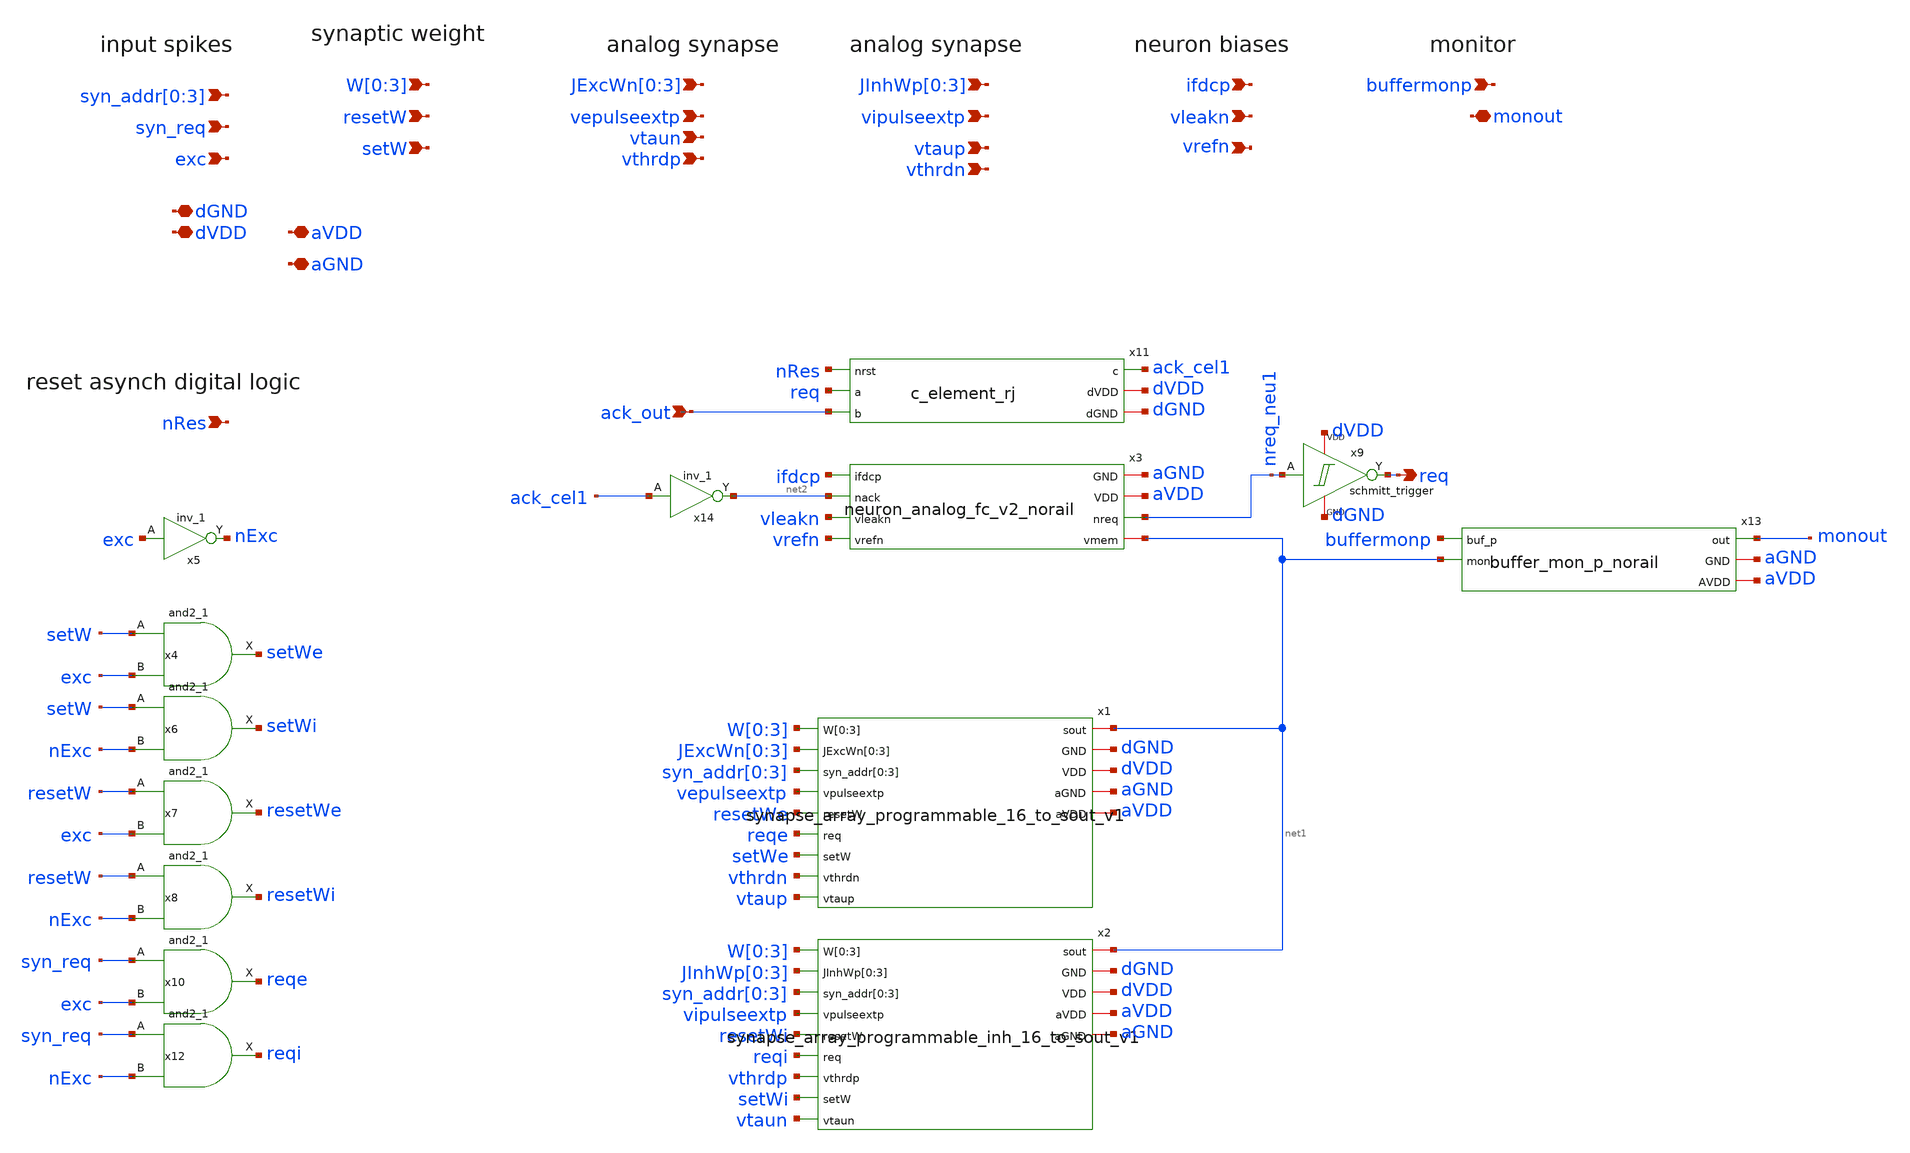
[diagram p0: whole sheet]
** sch_path: design/xschem/neuron_32syn_v1_norail.sch
**.subckt neuron_32syn_v1_norail ack_out dGND dVDD vepulseextp
*+ syn_addr[0],syn_addr[1],syn_addr[2],syn_addr[3] W[0],W[1],W[2],W[3] setW resetW syn_req exc vipulseextp req vleakn ifdcp vrefn nRes aVDD buffermonp
*+ monout JExcWn[0],JExcWn[1],JExcWn[2],JExcWn[3] JInhWp[0],JInhWp[1],JInhWp[2],JInhWp[3] vtaun vthrdp vtaup
*+ vthrdn aGND
*.ipin ack_out
*.iopin dGND
*.iopin dVDD
*.ipin vepulseextp
*.ipin syn_addr[0],syn_addr[1],syn_addr[2],syn_addr[3]
*.ipin W[0],W[1],W[2],W[3]
*.ipin setW
*.ipin resetW
*.ipin syn_req
*.ipin exc
*.ipin vipulseextp
*.opin req
*.ipin vleakn
*.ipin ifdcp
*.ipin vrefn
*.ipin nRes
*.iopin aVDD
*.ipin buffermonp
*.iopin monout
*.ipin JExcWn[0],JExcWn[1],JExcWn[2],JExcWn[3]
*.ipin JInhWp[0],JInhWp[1],JInhWp[2],JInhWp[3]
*.ipin vtaun
*.ipin vthrdp
*.ipin vtaup
*.ipin vthrdn
*.iopin aGND
x11 nRes req ack_out ack_cel1 dVDD dGND c_element_rj
x4 setW exc dGND dGND dVDD dVDD setWe sky130_fd_sc_hd__and2_1
x5 exc dGND dGND dVDD dVDD nExc sky130_fd_sc_hd__inv_1
x6 setW nExc dGND dGND dVDD dVDD setWi sky130_fd_sc_hd__and2_1
x7 resetW exc dGND dGND dVDD dVDD resetWe sky130_fd_sc_hd__and2_1
x8 resetW nExc dGND dGND dVDD dVDD resetWi sky130_fd_sc_hd__and2_1
x10 syn_req exc dGND dGND dVDD dVDD reqe sky130_fd_sc_hd__and2_1
x12 syn_req nExc dGND dGND dVDD dVDD reqi sky130_fd_sc_hd__and2_1
x14 ack_cel1 dGND dGND dVDD dVDD net2 sky130_fd_sc_hd__inv_1
x1 W[0] W[1] W[2] W[3] JExcWn[0] JExcWn[1] JExcWn[2] JExcWn[3] net1 syn_addr[0] syn_addr[1]
+ syn_addr[2] syn_addr[3] vepulseextp resetWe reqe setWe vthrdn vtaup dGND dVDD aGND aVDD
+ synapse_array_programmable_16_to_sout_v1
x2 net1 W[0] W[1] W[2] W[3] JInhWp[0] JInhWp[1] JInhWp[2] JInhWp[3] syn_addr[0] syn_addr[1]
+ syn_addr[2] syn_addr[3] vipulseextp resetWi reqi vthrdp setWi vtaun dGND dVDD aVDD aGND
+ synapse_array_programmable_inh_16_to_sout_v1
x9 nreq_neu1 req dVDD dGND schmitt_trigger
x3 aGND aVDD nreq_neu1 ifdcp net2 net1 vleakn vrefn neuron_analog_fc_v2_norail
x13 buffermonp monout net1 aGND aVDD buffer_mon_p_norail
**.ends

* expanding   symbol:  c_element_rj.sym # of pins=6
** sym_path: design/xschem/c_element_rj.sym
** sch_path: design/xschem/c_element_rj.sch
.subckt c_element_rj nrst a b c dVDD dGND
*.iopin dGND
*.iopin dVDD
*.opin c
*.ipin b
*.ipin a
*.ipin nrst
XM14 c net6 dVDD dVDD sky130_fd_pr__pfet_01v8 L=0.15 W=1 nf=1 ad='int((nf+1)/2) * W/nf * 0.29' as='int((nf+2)/2) * W/nf * 0.29'
+ pd='2*int((nf+1)/2) * (W/nf + 0.29)' ps='2*int((nf+2)/2) * (W/nf + 0.29)' nrd='0.29 / W' nrs='0.29 / W'
+ sa=0 sb=0 sd=0 mult=1 m=1
XM5 net6 nrst dVDD dVDD sky130_fd_pr__pfet_01v8 L=0.15 W=1 nf=1 ad='int((nf+1)/2) * W/nf * 0.29' as='int((nf+2)/2) * W/nf * 0.29'
+ pd='2*int((nf+1)/2) * (W/nf + 0.29)' ps='2*int((nf+2)/2) * (W/nf + 0.29)' nrd='0.29 / W' nrs='0.29 / W'
+ sa=0 sb=0 sd=0 mult=1 m=1
XM6 net5 b dVDD dVDD sky130_fd_pr__pfet_01v8 L=0.15 W=1 nf=1 ad='int((nf+1)/2) * W/nf * 0.29' as='int((nf+2)/2) * W/nf * 0.29'
+ pd='2*int((nf+1)/2) * (W/nf + 0.29)' ps='2*int((nf+2)/2) * (W/nf + 0.29)' nrd='0.29 / W' nrs='0.29 / W'
+ sa=0 sb=0 sd=0 mult=1 m=1
XM4 net4 a dVDD dVDD sky130_fd_pr__pfet_01v8 L=0.15 W=1 nf=1 ad='int((nf+1)/2) * W/nf * 0.29' as='int((nf+2)/2) * W/nf * 0.29'
+ pd='2*int((nf+1)/2) * (W/nf + 0.29)' ps='2*int((nf+2)/2) * (W/nf + 0.29)' nrd='0.29 / W' nrs='0.29 / W'
+ sa=0 sb=0 sd=0 mult=1 m=1
XM7 net3 b net4 dVDD sky130_fd_pr__pfet_01v8 L=0.15 W=1 nf=1 ad='int((nf+1)/2) * W/nf * 0.29' as='int((nf+2)/2) * W/nf * 0.29'
+ pd='2*int((nf+1)/2) * (W/nf + 0.29)' ps='2*int((nf+2)/2) * (W/nf + 0.29)' nrd='0.29 / W' nrs='0.29 / W'
+ sa=0 sb=0 sd=0 mult=1 m=1
XM8 net3 a net5 dVDD sky130_fd_pr__pfet_01v8 L=0.15 W=1 nf=1 ad='int((nf+1)/2) * W/nf * 0.29' as='int((nf+2)/2) * W/nf * 0.29'
+ pd='2*int((nf+1)/2) * (W/nf + 0.29)' ps='2*int((nf+2)/2) * (W/nf + 0.29)' nrd='0.29 / W' nrs='0.29 / W'
+ sa=0 sb=0 sd=0 mult=1 m=1
XM10 net5 c net4 dVDD sky130_fd_pr__pfet_01v8 L=0.15 W=1 nf=1 ad='int((nf+1)/2) * W/nf * 0.29' as='int((nf+2)/2) * W/nf * 0.29'
+ pd='2*int((nf+1)/2) * (W/nf + 0.29)' ps='2*int((nf+2)/2) * (W/nf + 0.29)' nrd='0.29 / W' nrs='0.29 / W'
+ sa=0 sb=0 sd=0 mult=1 m=1
XM12 c net6 dGND dGND sky130_fd_pr__nfet_01v8 L=0.15 W=0.65 nf=1 ad='int((nf+1)/2) * W/nf * 0.29' as='int((nf+2)/2) * W/nf * 0.29'
+ pd='2*int((nf+1)/2) * (W/nf + 0.29)' ps='2*int((nf+2)/2) * (W/nf + 0.29)' nrd='0.29 / W' nrs='0.29 / W'
+ sa=0 sb=0 sd=0 mult=1 m=1
XM1 net3 nrst net6 dGND sky130_fd_pr__nfet_01v8 L=0.15 W=0.65 nf=1 ad='int((nf+1)/2) * W/nf * 0.29' as='int((nf+2)/2) * W/nf * 0.29'
+ pd='2*int((nf+1)/2) * (W/nf + 0.29)' ps='2*int((nf+2)/2) * (W/nf + 0.29)' nrd='0.29 / W' nrs='0.29 / W'
+ sa=0 sb=0 sd=0 mult=1 m=1
XM2 net3 b net1 dGND sky130_fd_pr__nfet_01v8 L=0.15 W=0.65 nf=1 ad='int((nf+1)/2) * W/nf * 0.29' as='int((nf+2)/2) * W/nf * 0.29'
+ pd='2*int((nf+1)/2) * (W/nf + 0.29)' ps='2*int((nf+2)/2) * (W/nf + 0.29)' nrd='0.29 / W' nrs='0.29 / W'
+ sa=0 sb=0 sd=0 mult=1 m=1
XM3 net3 a net2 dGND sky130_fd_pr__nfet_01v8 L=0.15 W=0.65 nf=1 ad='int((nf+1)/2) * W/nf * 0.29' as='int((nf+2)/2) * W/nf * 0.29'
+ pd='2*int((nf+1)/2) * (W/nf + 0.29)' ps='2*int((nf+2)/2) * (W/nf + 0.29)' nrd='0.29 / W' nrs='0.29 / W'
+ sa=0 sb=0 sd=0 mult=1 m=1
XM9 net2 c net1 dGND sky130_fd_pr__nfet_01v8 L=0.15 W=0.65 nf=1 ad='int((nf+1)/2) * W/nf * 0.29' as='int((nf+2)/2) * W/nf * 0.29'
+ pd='2*int((nf+1)/2) * (W/nf + 0.29)' ps='2*int((nf+2)/2) * (W/nf + 0.29)' nrd='0.29 / W' nrs='0.29 / W'
+ sa=0 sb=0 sd=0 mult=1 m=1
XM11 net1 a dGND dGND sky130_fd_pr__nfet_01v8 L=0.15 W=0.65 nf=1 ad='int((nf+1)/2) * W/nf * 0.29' as='int((nf+2)/2) * W/nf * 0.29'
+ pd='2*int((nf+1)/2) * (W/nf + 0.29)' ps='2*int((nf+2)/2) * (W/nf + 0.29)' nrd='0.29 / W' nrs='0.29 / W'
+ sa=0 sb=0 sd=0 mult=1 m=1
XM13 net2 b dGND dGND sky130_fd_pr__nfet_01v8 L=0.15 W=0.65 nf=1 ad='int((nf+1)/2) * W/nf * 0.29' as='int((nf+2)/2) * W/nf * 0.29'
+ pd='2*int((nf+1)/2) * (W/nf + 0.29)' ps='2*int((nf+2)/2) * (W/nf + 0.29)' nrd='0.29 / W' nrs='0.29 / W'
+ sa=0 sb=0 sd=0 mult=1 m=1
.ends


* expanding   symbol:  synapse_array_programmable_16_to_sout_v1.sym # of pins=14
** sym_path: design/xschem/synapse_array_programmable_16_to_sout_v1.sym
** sch_path: design/xschem/synapse_array_programmable_16_to_sout_v1.sch
.subckt synapse_array_programmable_16_to_sout_v1 W[0] W[1] W[2] W[3] JExcWn[0] JExcWn[1] JExcWn[2]
+ JExcWn[3] sout syn_addr[0] syn_addr[1] syn_addr[2] syn_addr[3] vpulseextp resetW req setW vthrdn vtaup GND
+ VDD aGND aVDD
*.iopin GND
*.iopin VDD
*.ipin vpulseextp
*.ipin syn_addr[0],syn_addr[1],syn_addr[2],syn_addr[3]
*.ipin W[0],W[1],W[2],W[3]
*.ipin JExcWn[0],JExcWn[1],JExcWn[2],JExcWn[3]
*.iopin sout
*.ipin setW
*.ipin resetW
*.ipin req
*.ipin vthrdn
*.ipin vtaup
*.iopin aVDD
*.iopin aGND
x3 syn_addr[0] syn_addr[1] syn_addr[2] syn_addr[3] D[0] D[1] D[2] D[3] D[4] D[5] D[6] D[7] D[8] D[9]
+ D[10] D[11] D[12] D[13] D[14] D[15] req req_syn VDD GND decoder_4_to_16
x2[0] req_syn D[0] GND GND VDD VDD net1[15] sky130_fd_sc_hd__and2_1
x2[1] req_syn D[1] GND GND VDD VDD net1[14] sky130_fd_sc_hd__and2_1
x2[2] req_syn D[2] GND GND VDD VDD net1[13] sky130_fd_sc_hd__and2_1
x2[3] req_syn D[3] GND GND VDD VDD net1[12] sky130_fd_sc_hd__and2_1
x2[4] req_syn D[4] GND GND VDD VDD net1[11] sky130_fd_sc_hd__and2_1
x2[5] req_syn D[5] GND GND VDD VDD net1[10] sky130_fd_sc_hd__and2_1
x2[6] req_syn D[6] GND GND VDD VDD net1[9] sky130_fd_sc_hd__and2_1
x2[7] req_syn D[7] GND GND VDD VDD net1[8] sky130_fd_sc_hd__and2_1
x2[8] req_syn D[8] GND GND VDD VDD net1[7] sky130_fd_sc_hd__and2_1
x2[9] req_syn D[9] GND GND VDD VDD net1[6] sky130_fd_sc_hd__and2_1
x2[10] req_syn D[10] GND GND VDD VDD net1[5] sky130_fd_sc_hd__and2_1
x2[11] req_syn D[11] GND GND VDD VDD net1[4] sky130_fd_sc_hd__and2_1
x2[12] req_syn D[12] GND GND VDD VDD net1[3] sky130_fd_sc_hd__and2_1
x2[13] req_syn D[13] GND GND VDD VDD net1[2] sky130_fd_sc_hd__and2_1
x2[14] req_syn D[14] GND GND VDD VDD net1[1] sky130_fd_sc_hd__and2_1
x2[15] req_syn D[15] GND GND VDD VDD net1[0] sky130_fd_sc_hd__and2_1
x1[0] sout JExcWn[0] JExcWn[1] JExcWn[2] JExcWn[3] net1[15] resetW vpulseextp net2[15] vthrdn W[0]
+ W[1] W[2] W[3] vtaup VDD GND aVDD aGND synapse_4bit_memory_v1_norail
x1[1] sout JExcWn[0] JExcWn[1] JExcWn[2] JExcWn[3] net1[14] resetW vpulseextp net2[14] vthrdn W[0]
+ W[1] W[2] W[3] vtaup VDD GND aVDD aGND synapse_4bit_memory_v1_norail
x1[2] sout JExcWn[0] JExcWn[1] JExcWn[2] JExcWn[3] net1[13] resetW vpulseextp net2[13] vthrdn W[0]
+ W[1] W[2] W[3] vtaup VDD GND aVDD aGND synapse_4bit_memory_v1_norail
x1[3] sout JExcWn[0] JExcWn[1] JExcWn[2] JExcWn[3] net1[12] resetW vpulseextp net2[12] vthrdn W[0]
+ W[1] W[2] W[3] vtaup VDD GND aVDD aGND synapse_4bit_memory_v1_norail
x1[4] sout JExcWn[0] JExcWn[1] JExcWn[2] JExcWn[3] net1[11] resetW vpulseextp net2[11] vthrdn W[0]
+ W[1] W[2] W[3] vtaup VDD GND aVDD aGND synapse_4bit_memory_v1_norail
x1[5] sout JExcWn[0] JExcWn[1] JExcWn[2] JExcWn[3] net1[10] resetW vpulseextp net2[10] vthrdn W[0]
+ W[1] W[2] W[3] vtaup VDD GND aVDD aGND synapse_4bit_memory_v1_norail
x1[6] sout JExcWn[0] JExcWn[1] JExcWn[2] JExcWn[3] net1[9] resetW vpulseextp net2[9] vthrdn W[0]
+ W[1] W[2] W[3] vtaup VDD GND aVDD aGND synapse_4bit_memory_v1_norail
x1[7] sout JExcWn[0] JExcWn[1] JExcWn[2] JExcWn[3] net1[8] resetW vpulseextp net2[8] vthrdn W[0]
+ W[1] W[2] W[3] vtaup VDD GND aVDD aGND synapse_4bit_memory_v1_norail
x1[8] sout JExcWn[0] JExcWn[1] JExcWn[2] JExcWn[3] net1[7] resetW vpulseextp net2[7] vthrdn W[0]
+ W[1] W[2] W[3] vtaup VDD GND aVDD aGND synapse_4bit_memory_v1_norail
x1[9] sout JExcWn[0] JExcWn[1] JExcWn[2] JExcWn[3] net1[6] resetW vpulseextp net2[6] vthrdn W[0]
+ W[1] W[2] W[3] vtaup VDD GND aVDD aGND synapse_4bit_memory_v1_norail
x1[10] sout JExcWn[0] JExcWn[1] JExcWn[2] JExcWn[3] net1[5] resetW vpulseextp net2[5] vthrdn W[0]
+ W[1] W[2] W[3] vtaup VDD GND aVDD aGND synapse_4bit_memory_v1_norail
x1[11] sout JExcWn[0] JExcWn[1] JExcWn[2] JExcWn[3] net1[4] resetW vpulseextp net2[4] vthrdn W[0]
+ W[1] W[2] W[3] vtaup VDD GND aVDD aGND synapse_4bit_memory_v1_norail
x1[12] sout JExcWn[0] JExcWn[1] JExcWn[2] JExcWn[3] net1[3] resetW vpulseextp net2[3] vthrdn W[0]
+ W[1] W[2] W[3] vtaup VDD GND aVDD aGND synapse_4bit_memory_v1_norail
x1[13] sout JExcWn[0] JExcWn[1] JExcWn[2] JExcWn[3] net1[2] resetW vpulseextp net2[2] vthrdn W[0]
+ W[1] W[2] W[3] vtaup VDD GND aVDD aGND synapse_4bit_memory_v1_norail
x1[14] sout JExcWn[0] JExcWn[1] JExcWn[2] JExcWn[3] net1[1] resetW vpulseextp net2[1] vthrdn W[0]
+ W[1] W[2] W[3] vtaup VDD GND aVDD aGND synapse_4bit_memory_v1_norail
x1[15] sout JExcWn[0] JExcWn[1] JExcWn[2] JExcWn[3] net1[0] resetW vpulseextp net2[0] vthrdn W[0]
+ W[1] W[2] W[3] vtaup VDD GND aVDD aGND synapse_4bit_memory_v1_norail
x3[0] D[0] setW GND GND VDD VDD net2[15] sky130_fd_sc_hd__and2_1
x3[1] D[1] setW GND GND VDD VDD net2[14] sky130_fd_sc_hd__and2_1
x3[2] D[2] setW GND GND VDD VDD net2[13] sky130_fd_sc_hd__and2_1
x3[3] D[3] setW GND GND VDD VDD net2[12] sky130_fd_sc_hd__and2_1
x3[4] D[4] setW GND GND VDD VDD net2[11] sky130_fd_sc_hd__and2_1
x3[5] D[5] setW GND GND VDD VDD net2[10] sky130_fd_sc_hd__and2_1
x3[6] D[6] setW GND GND VDD VDD net2[9] sky130_fd_sc_hd__and2_1
x3[7] D[7] setW GND GND VDD VDD net2[8] sky130_fd_sc_hd__and2_1
x3[8] D[8] setW GND GND VDD VDD net2[7] sky130_fd_sc_hd__and2_1
x3[9] D[9] setW GND GND VDD VDD net2[6] sky130_fd_sc_hd__and2_1
x3[10] D[10] setW GND GND VDD VDD net2[5] sky130_fd_sc_hd__and2_1
x3[11] D[11] setW GND GND VDD VDD net2[4] sky130_fd_sc_hd__and2_1
x3[12] D[12] setW GND GND VDD VDD net2[3] sky130_fd_sc_hd__and2_1
x3[13] D[13] setW GND GND VDD VDD net2[2] sky130_fd_sc_hd__and2_1
x3[14] D[14] setW GND GND VDD VDD net2[1] sky130_fd_sc_hd__and2_1
x3[15] D[15] setW GND GND VDD VDD net2[0] sky130_fd_sc_hd__and2_1
.ends


* expanding   symbol:  synapse_array_programmable_inh_16_to_sout_v1.sym # of pins=14
** sym_path: design/xschem/synapse_array_programmable_inh_16_to_sout_v1.sym
** sch_path: design/xschem/synapse_array_programmable_inh_16_to_sout_v1.sch
.subckt synapse_array_programmable_inh_16_to_sout_v1 sout W[0] W[1] W[2] W[3] JInhWp[0] JInhWp[1]
+ JInhWp[2] JInhWp[3] syn_addr[0] syn_addr[1] syn_addr[2] syn_addr[3] vpulseextp resetW req vthrdp setW vtaun
+ GND VDD aVDD aGND
*.ipin vpulseextp
*.ipin syn_addr[0],syn_addr[1],syn_addr[2],syn_addr[3]
*.ipin W[0],W[1],W[2],W[3]
*.ipin JInhWp[0],JInhWp[1],JInhWp[2],JInhWp[3]
*.iopin sout
*.ipin setW
*.ipin resetW
*.ipin req
*.ipin vthrdp
*.ipin vtaun
*.iopin GND
*.iopin VDD
*.iopin aVDD
*.iopin aGND
x3 syn_addr[0] syn_addr[1] syn_addr[2] syn_addr[3] D[0] D[1] D[2] D[3] D[4] D[5] D[6] D[7] D[8] D[9]
+ D[10] D[11] D[12] D[13] D[14] D[15] req req_syn VDD GND decoder_4_to_16
x2[0] req_syn D[0] GND GND VDD VDD net1[15] sky130_fd_sc_hd__and2_1
x2[1] req_syn D[1] GND GND VDD VDD net1[14] sky130_fd_sc_hd__and2_1
x2[2] req_syn D[2] GND GND VDD VDD net1[13] sky130_fd_sc_hd__and2_1
x2[3] req_syn D[3] GND GND VDD VDD net1[12] sky130_fd_sc_hd__and2_1
x2[4] req_syn D[4] GND GND VDD VDD net1[11] sky130_fd_sc_hd__and2_1
x2[5] req_syn D[5] GND GND VDD VDD net1[10] sky130_fd_sc_hd__and2_1
x2[6] req_syn D[6] GND GND VDD VDD net1[9] sky130_fd_sc_hd__and2_1
x2[7] req_syn D[7] GND GND VDD VDD net1[8] sky130_fd_sc_hd__and2_1
x2[8] req_syn D[8] GND GND VDD VDD net1[7] sky130_fd_sc_hd__and2_1
x2[9] req_syn D[9] GND GND VDD VDD net1[6] sky130_fd_sc_hd__and2_1
x2[10] req_syn D[10] GND GND VDD VDD net1[5] sky130_fd_sc_hd__and2_1
x2[11] req_syn D[11] GND GND VDD VDD net1[4] sky130_fd_sc_hd__and2_1
x2[12] req_syn D[12] GND GND VDD VDD net1[3] sky130_fd_sc_hd__and2_1
x2[13] req_syn D[13] GND GND VDD VDD net1[2] sky130_fd_sc_hd__and2_1
x2[14] req_syn D[14] GND GND VDD VDD net1[1] sky130_fd_sc_hd__and2_1
x2[15] req_syn D[15] GND GND VDD VDD net1[0] sky130_fd_sc_hd__and2_1
x3[0] D[0] setW GND GND VDD VDD net2[15] sky130_fd_sc_hd__and2_1
x3[1] D[1] setW GND GND VDD VDD net2[14] sky130_fd_sc_hd__and2_1
x3[2] D[2] setW GND GND VDD VDD net2[13] sky130_fd_sc_hd__and2_1
x3[3] D[3] setW GND GND VDD VDD net2[12] sky130_fd_sc_hd__and2_1
x3[4] D[4] setW GND GND VDD VDD net2[11] sky130_fd_sc_hd__and2_1
x3[5] D[5] setW GND GND VDD VDD net2[10] sky130_fd_sc_hd__and2_1
x3[6] D[6] setW GND GND VDD VDD net2[9] sky130_fd_sc_hd__and2_1
x3[7] D[7] setW GND GND VDD VDD net2[8] sky130_fd_sc_hd__and2_1
x3[8] D[8] setW GND GND VDD VDD net2[7] sky130_fd_sc_hd__and2_1
x3[9] D[9] setW GND GND VDD VDD net2[6] sky130_fd_sc_hd__and2_1
x3[10] D[10] setW GND GND VDD VDD net2[5] sky130_fd_sc_hd__and2_1
x3[11] D[11] setW GND GND VDD VDD net2[4] sky130_fd_sc_hd__and2_1
x3[12] D[12] setW GND GND VDD VDD net2[3] sky130_fd_sc_hd__and2_1
x3[13] D[13] setW GND GND VDD VDD net2[2] sky130_fd_sc_hd__and2_1
x3[14] D[14] setW GND GND VDD VDD net2[1] sky130_fd_sc_hd__and2_1
x3[15] D[15] setW GND GND VDD VDD net2[0] sky130_fd_sc_hd__and2_1
x1[0] sout JInhWp[0] JInhWp[1] JInhWp[2] JInhWp[3] resetW net1[15] vpulseextp net2[15] vthrdp W[0]
+ W[1] W[2] W[3] vtaun GND VDD aVDD aGND synapse_4bit_memory_inh_v1_norail
x1[1] sout JInhWp[0] JInhWp[1] JInhWp[2] JInhWp[3] resetW net1[14] vpulseextp net2[14] vthrdp W[0]
+ W[1] W[2] W[3] vtaun GND VDD aVDD aGND synapse_4bit_memory_inh_v1_norail
x1[2] sout JInhWp[0] JInhWp[1] JInhWp[2] JInhWp[3] resetW net1[13] vpulseextp net2[13] vthrdp W[0]
+ W[1] W[2] W[3] vtaun GND VDD aVDD aGND synapse_4bit_memory_inh_v1_norail
x1[3] sout JInhWp[0] JInhWp[1] JInhWp[2] JInhWp[3] resetW net1[12] vpulseextp net2[12] vthrdp W[0]
+ W[1] W[2] W[3] vtaun GND VDD aVDD aGND synapse_4bit_memory_inh_v1_norail
x1[4] sout JInhWp[0] JInhWp[1] JInhWp[2] JInhWp[3] resetW net1[11] vpulseextp net2[11] vthrdp W[0]
+ W[1] W[2] W[3] vtaun GND VDD aVDD aGND synapse_4bit_memory_inh_v1_norail
x1[5] sout JInhWp[0] JInhWp[1] JInhWp[2] JInhWp[3] resetW net1[10] vpulseextp net2[10] vthrdp W[0]
+ W[1] W[2] W[3] vtaun GND VDD aVDD aGND synapse_4bit_memory_inh_v1_norail
x1[6] sout JInhWp[0] JInhWp[1] JInhWp[2] JInhWp[3] resetW net1[9] vpulseextp net2[9] vthrdp W[0]
+ W[1] W[2] W[3] vtaun GND VDD aVDD aGND synapse_4bit_memory_inh_v1_norail
x1[7] sout JInhWp[0] JInhWp[1] JInhWp[2] JInhWp[3] resetW net1[8] vpulseextp net2[8] vthrdp W[0]
+ W[1] W[2] W[3] vtaun GND VDD aVDD aGND synapse_4bit_memory_inh_v1_norail
x1[8] sout JInhWp[0] JInhWp[1] JInhWp[2] JInhWp[3] resetW net1[7] vpulseextp net2[7] vthrdp W[0]
+ W[1] W[2] W[3] vtaun GND VDD aVDD aGND synapse_4bit_memory_inh_v1_norail
x1[9] sout JInhWp[0] JInhWp[1] JInhWp[2] JInhWp[3] resetW net1[6] vpulseextp net2[6] vthrdp W[0]
+ W[1] W[2] W[3] vtaun GND VDD aVDD aGND synapse_4bit_memory_inh_v1_norail
x1[10] sout JInhWp[0] JInhWp[1] JInhWp[2] JInhWp[3] resetW net1[5] vpulseextp net2[5] vthrdp W[0]
+ W[1] W[2] W[3] vtaun GND VDD aVDD aGND synapse_4bit_memory_inh_v1_norail
x1[11] sout JInhWp[0] JInhWp[1] JInhWp[2] JInhWp[3] resetW net1[4] vpulseextp net2[4] vthrdp W[0]
+ W[1] W[2] W[3] vtaun GND VDD aVDD aGND synapse_4bit_memory_inh_v1_norail
x1[12] sout JInhWp[0] JInhWp[1] JInhWp[2] JInhWp[3] resetW net1[3] vpulseextp net2[3] vthrdp W[0]
+ W[1] W[2] W[3] vtaun GND VDD aVDD aGND synapse_4bit_memory_inh_v1_norail
x1[13] sout JInhWp[0] JInhWp[1] JInhWp[2] JInhWp[3] resetW net1[2] vpulseextp net2[2] vthrdp W[0]
+ W[1] W[2] W[3] vtaun GND VDD aVDD aGND synapse_4bit_memory_inh_v1_norail
x1[14] sout JInhWp[0] JInhWp[1] JInhWp[2] JInhWp[3] resetW net1[1] vpulseextp net2[1] vthrdp W[0]
+ W[1] W[2] W[3] vtaun GND VDD aVDD aGND synapse_4bit_memory_inh_v1_norail
x1[15] sout JInhWp[0] JInhWp[1] JInhWp[2] JInhWp[3] resetW net1[0] vpulseextp net2[0] vthrdp W[0]
+ W[1] W[2] W[3] vtaun GND VDD aVDD aGND synapse_4bit_memory_inh_v1_norail
.ends


* expanding   symbol:  schmitt_trigger.sym # of pins=4
** sym_path: design/xschem/schmitt_trigger.sym
** sch_path: design/xschem/schmitt_trigger.sch
.subckt schmitt_trigger A Y VDD GND
*.ipin A
*.opin Y
*.iopin VDD
*.iopin GND
XM3 net2 A GND GND sky130_fd_pr__nfet_01v8 L=0.15 W=0.65 nf=1 ad='int((nf+1)/2) * W/nf * 0.29' as='int((nf+2)/2) * W/nf * 0.29'
+ pd='2*int((nf+1)/2) * (W/nf + 0.29)' ps='2*int((nf+2)/2) * (W/nf + 0.29)' nrd='0.29 / W' nrs='0.29 / W'
+ sa=0 sb=0 sd=0 mult=1 m=1
XM1 Y A net2 GND sky130_fd_pr__nfet_01v8 L=0.15 W=0.65 nf=1 ad='int((nf+1)/2) * W/nf * 0.29' as='int((nf+2)/2) * W/nf * 0.29'
+ pd='2*int((nf+1)/2) * (W/nf + 0.29)' ps='2*int((nf+2)/2) * (W/nf + 0.29)' nrd='0.29 / W' nrs='0.29 / W'
+ sa=0 sb=0 sd=0 mult=1 m=1
XM7 VDD Y net2 GND sky130_fd_pr__nfet_01v8 L=0.15 W=0.42 nf=1 ad='int((nf+1)/2) * W/nf * 0.29' as='int((nf+2)/2) * W/nf * 0.29'
+ pd='2*int((nf+1)/2) * (W/nf + 0.29)' ps='2*int((nf+2)/2) * (W/nf + 0.29)' nrd='0.29 / W' nrs='0.29 / W'
+ sa=0 sb=0 sd=0 mult=1 m=1
XM4 net1 A VDD VDD sky130_fd_pr__pfet_01v8 L=0.15 W=1 nf=1 ad='int((nf+1)/2) * W/nf * 0.29' as='int((nf+2)/2) * W/nf * 0.29'
+ pd='2*int((nf+1)/2) * (W/nf + 0.29)' ps='2*int((nf+2)/2) * (W/nf + 0.29)' nrd='0.29 / W' nrs='0.29 / W'
+ sa=0 sb=0 sd=0 mult=1 m=1
XM2 Y A net1 VDD sky130_fd_pr__pfet_01v8 L=0.15 W=1 nf=1 ad='int((nf+1)/2) * W/nf * 0.29' as='int((nf+2)/2) * W/nf * 0.29'
+ pd='2*int((nf+1)/2) * (W/nf + 0.29)' ps='2*int((nf+2)/2) * (W/nf + 0.29)' nrd='0.29 / W' nrs='0.29 / W'
+ sa=0 sb=0 sd=0 mult=1 m=1
XM5 GND Y net1 VDD sky130_fd_pr__pfet_01v8 L=0.15 W=0.82 nf=1 ad='int((nf+1)/2) * W/nf * 0.29' as='int((nf+2)/2) * W/nf * 0.29'
+ pd='2*int((nf+1)/2) * (W/nf + 0.29)' ps='2*int((nf+2)/2) * (W/nf + 0.29)' nrd='0.29 / W' nrs='0.29 / W'
+ sa=0 sb=0 sd=0 mult=1 m=1
.ends


* expanding   symbol:  neuron_analog_fc_v2_norail.sym # of pins=8
** sym_path: design/xschem/neuron_analog_fc_v2_norail.sym
** sch_path: design/xschem/neuron_analog_fc_v2_norail.sch
.subckt neuron_analog_fc_v2_norail GND VDD nreq ifdcp nack vmem vleakn vrefn
*.ipin vleakn
*.iopin GND
*.iopin VDD
*.opin nreq
*.ipin vrefn
*.ipin nack
*.ipin ifdcp
*.iopin vmem
XC1 GND vmem sky130_fd_pr__cap_mim_m3_1 W=5 L=5 MF=1 m=1
XM1 vmem ifdcp VDD VDD sky130_fd_pr__pfet_01v8 L=2.0 W=1.0 nf=1 ad='int((nf+1)/2) * W/nf * 0.29' as='int((nf+2)/2) * W/nf * 0.29'
+ pd='2*int((nf+1)/2) * (W/nf + 0.29)' ps='2*int((nf+2)/2) * (W/nf + 0.29)' nrd='0.29 / W' nrs='0.29 / W'
+ sa=0 sb=0 sd=0 mult=1 m=1
XM5 net2 nreq VDD VDD sky130_fd_pr__pfet_01v8 L=0.25 W=1.0 nf=1 ad='int((nf+1)/2) * W/nf * 0.29' as='int((nf+2)/2) * W/nf * 0.29'
+ pd='2*int((nf+1)/2) * (W/nf + 0.29)' ps='2*int((nf+2)/2) * (W/nf + 0.29)' nrd='0.29 / W' nrs='0.29 / W'
+ sa=0 sb=0 sd=0 mult=1 m=1
XM7 net3 nreq net4 GND sky130_fd_pr__nfet_01v8 L=0.15 W=0.6 nf=1 ad='int((nf+1)/2) * W/nf * 0.29' as='int((nf+2)/2) * W/nf * 0.29'
+ pd='2*int((nf+1)/2) * (W/nf + 0.29)' ps='2*int((nf+2)/2) * (W/nf + 0.29)' nrd='0.29 / W' nrs='0.29 / W'
+ sa=0 sb=0 sd=0 mult=1 m=1
XM6 net5 nack VDD VDD sky130_fd_pr__pfet_01v8 L=0.25 W=1.0 nf=1 ad='int((nf+1)/2) * W/nf * 0.29' as='int((nf+2)/2) * W/nf * 0.29'
+ pd='2*int((nf+1)/2) * (W/nf + 0.29)' ps='2*int((nf+2)/2) * (W/nf + 0.29)' nrd='0.29 / W' nrs='0.29 / W'
+ sa=0 sb=0 sd=0 mult=1 m=1
XM9 nreq vmem net2 VDD sky130_fd_pr__pfet_01v8 L=0.15 W=1.0 nf=1 ad='int((nf+1)/2) * W/nf * 0.29' as='int((nf+2)/2) * W/nf * 0.29'
+ pd='2*int((nf+1)/2) * (W/nf + 0.29)' ps='2*int((nf+2)/2) * (W/nf + 0.29)' nrd='0.29 / W' nrs='0.29 / W'
+ sa=0 sb=0 sd=0 mult=1 m=1
XM10 net3 nreq net5 VDD sky130_fd_pr__pfet_01v8 L=0.15 W=1.0 nf=1 ad='int((nf+1)/2) * W/nf * 0.29' as='int((nf+2)/2) * W/nf * 0.29'
+ pd='2*int((nf+1)/2) * (W/nf + 0.29)' ps='2*int((nf+2)/2) * (W/nf + 0.29)' nrd='0.29 / W' nrs='0.29 / W'
+ sa=0 sb=0 sd=0 mult=1 m=1
XM4 vmem nreq VDD VDD sky130_fd_pr__pfet_01v8 L=1.0 W=1.0 nf=1 ad='int((nf+1)/2) * W/nf * 0.29' as='int((nf+2)/2) * W/nf * 0.29'
+ pd='2*int((nf+1)/2) * (W/nf + 0.29)' ps='2*int((nf+2)/2) * (W/nf + 0.29)' nrd='0.29 / W' nrs='0.29 / W'
+ sa=0 sb=0 sd=0 mult=1 m=1
XM2 nreq vmem net1 GND sky130_fd_pr__nfet_01v8 L=0.15 W=0.6 nf=1 ad='int((nf+1)/2) * W/nf * 0.29' as='int((nf+2)/2) * W/nf * 0.29'
+ pd='2*int((nf+1)/2) * (W/nf + 0.29)' ps='2*int((nf+2)/2) * (W/nf + 0.29)' nrd='0.29 / W' nrs='0.29 / W'
+ sa=0 sb=0 sd=0 mult=1 m=1
XM3 net4 vrefn GND GND sky130_fd_pr__nfet_01v8 L=1.0 W=0.6 nf=1 ad='int((nf+1)/2) * W/nf * 0.29' as='int((nf+2)/2) * W/nf * 0.29'
+ pd='2*int((nf+1)/2) * (W/nf + 0.29)' ps='2*int((nf+2)/2) * (W/nf + 0.29)' nrd='0.29 / W' nrs='0.29 / W'
+ sa=0 sb=0 sd=0 mult=1 m=1
XM8 net1 net1 GND GND sky130_fd_pr__nfet_01v8 L=0.15 W=0.6 nf=1 ad='int((nf+1)/2) * W/nf * 0.29' as='int((nf+2)/2) * W/nf * 0.29'
+ pd='2*int((nf+1)/2) * (W/nf + 0.29)' ps='2*int((nf+2)/2) * (W/nf + 0.29)' nrd='0.29 / W' nrs='0.29 / W'
+ sa=0 sb=0 sd=0 mult=1 m=1
XM11 vmem net3 GND GND sky130_fd_pr__nfet_01v8 L=0.2 W=1.0 nf=1 ad='int((nf+1)/2) * W/nf * 0.29' as='int((nf+2)/2) * W/nf * 0.29'
+ pd='2*int((nf+1)/2) * (W/nf + 0.29)' ps='2*int((nf+2)/2) * (W/nf + 0.29)' nrd='0.29 / W' nrs='0.29 / W'
+ sa=0 sb=0 sd=0 mult=1 m=1
XM12 vmem vleakn GND GND sky130_fd_pr__nfet_01v8 L=2.0 W=1.0 nf=1 ad='int((nf+1)/2) * W/nf * 0.29' as='int((nf+2)/2) * W/nf * 0.29'
+ pd='2*int((nf+1)/2) * (W/nf + 0.29)' ps='2*int((nf+2)/2) * (W/nf + 0.29)' nrd='0.29 / W' nrs='0.29 / W'
+ sa=0 sb=0 sd=0 mult=1 m=1
XM13 GND net3 GND GND sky130_fd_pr__nfet_01v8 L=2.0 W=1.0 nf=1 ad='int((nf+1)/2) * W/nf * 0.29' as='int((nf+2)/2) * W/nf * 0.29'
+ pd='2*int((nf+1)/2) * (W/nf + 0.29)' ps='2*int((nf+2)/2) * (W/nf + 0.29)' nrd='0.29 / W' nrs='0.29 / W'
+ sa=0 sb=0 sd=0 mult=1 m=1
.ends


* expanding   symbol:  buffer_mon_p_norail.sym # of pins=5
** sym_path: design/xschem/buffer_mon_p_norail.sym
** sch_path: design/xschem/buffer_mon_p_norail.sch
.subckt buffer_mon_p_norail buf_p out mon GND AVDD
*.iopin GND
*.iopin AVDD
*.ipin buf_p
*.ipin mon
*.opin out
XM1 out out net2 AVDD sky130_fd_pr__pfet_01v8 L=0.5 W=1.0 nf=1 ad='int((nf+1)/2) * W/nf * 0.29' as='int((nf+2)/2) * W/nf * 0.29'
+ pd='2*int((nf+1)/2) * (W/nf + 0.29)' ps='2*int((nf+2)/2) * (W/nf + 0.29)' nrd='0.29 / W' nrs='0.29 / W'
+ sa=0 sb=0 sd=0 mult=1 m=1
XM5 net1 mon net2 AVDD sky130_fd_pr__pfet_01v8 L=0.5 W=1.0 nf=1 ad='int((nf+1)/2) * W/nf * 0.29' as='int((nf+2)/2) * W/nf * 0.29'
+ pd='2*int((nf+1)/2) * (W/nf + 0.29)' ps='2*int((nf+2)/2) * (W/nf + 0.29)' nrd='0.29 / W' nrs='0.29 / W'
+ sa=0 sb=0 sd=0 mult=1 m=1
XM2 net2 buf_p AVDD AVDD sky130_fd_pr__pfet_01v8 L=0.30 W=1.0 nf=1 ad='int((nf+1)/2) * W/nf * 0.29' as='int((nf+2)/2) * W/nf * 0.29'
+ pd='2*int((nf+1)/2) * (W/nf + 0.29)' ps='2*int((nf+2)/2) * (W/nf + 0.29)' nrd='0.29 / W' nrs='0.29 / W'
+ sa=0 sb=0 sd=0 mult=1 m=1
XM3 out net1 GND GND sky130_fd_pr__nfet_01v8 L=0.5 W=1.0 nf=1 ad='int((nf+1)/2) * W/nf * 0.29' as='int((nf+2)/2) * W/nf * 0.29'
+ pd='2*int((nf+1)/2) * (W/nf + 0.29)' ps='2*int((nf+2)/2) * (W/nf + 0.29)' nrd='0.29 / W' nrs='0.29 / W'
+ sa=0 sb=0 sd=0 mult=1 m=1
XM4 net1 net1 GND GND sky130_fd_pr__nfet_01v8 L=0.5 W=1.0 nf=1 ad='int((nf+1)/2) * W/nf * 0.29' as='int((nf+2)/2) * W/nf * 0.29'
+ pd='2*int((nf+1)/2) * (W/nf + 0.29)' ps='2*int((nf+2)/2) * (W/nf + 0.29)' nrd='0.29 / W' nrs='0.29 / W'
+ sa=0 sb=0 sd=0 mult=1 m=1
.ends


* expanding   symbol:  decoder_4_to_16.sym # of pins=6
** sym_path: design/xschem/decoder_4_to_16.sym
** sch_path: design/xschem/decoder_4_to_16.sch
.subckt decoder_4_to_16 A[0] A[1] A[2] A[3] D[0] D[1] D[2] D[3] D[4] D[5] D[6] D[7] D[8] D[9] D[10]
+ D[11] D[12] D[13] D[14] D[15] req req_syn dVDD dGND
*.ipin A[0],A[1],A[2],A[3]
*.ipin req
*.opin D[0],D[1],D[2],D[3],D[4],D[5],D[6],D[7],D[8],D[9],D[10],D[11],D[12],D[13],D[14],D[15]
*.opin req_syn
*.iopin dVDD
*.iopin dGND
x21 req dGND dGND dVDD dVDD net5 sky130_fd_sc_hd__inv_1
x22 net5 dGND dGND dVDD dVDD net6 sky130_fd_sc_hd__inv_1
x23 net6 dGND dGND dVDD dVDD net7 sky130_fd_sc_hd__inv_1
x24 net7 dGND dGND dVDD dVDD req_syn sky130_fd_sc_hd__inv_1
x20 A[3] A[2] A[1] A[0] dGND dGND dVDD dVDD D[15] sky130_fd_sc_hd__and4_1
x19 A[3] A[2] A[1] net4 dGND dGND dVDD dVDD D[14] sky130_fd_sc_hd__and4_1
x18 A[3] A[2] net3 A[0] dGND dGND dVDD dVDD D[13] sky130_fd_sc_hd__and4_1
x17 A[3] A[2] net3 net4 dGND dGND dVDD dVDD D[12] sky130_fd_sc_hd__and4_1
x16 A[3] net2 A[1] A[0] dGND dGND dVDD dVDD D[11] sky130_fd_sc_hd__and4_1
x15 A[3] net2 A[1] net4 dGND dGND dVDD dVDD D[10] sky130_fd_sc_hd__and4_1
x13 A[3] net2 net3 A[0] dGND dGND dVDD dVDD D[9] sky130_fd_sc_hd__and4_1
x4 A[3] net2 net3 net4 dGND dGND dVDD dVDD D[8] sky130_fd_sc_hd__and4_1
x5 net1 A[2] A[1] A[0] dGND dGND dVDD dVDD D[7] sky130_fd_sc_hd__and4_1
x6 net1 A[2] A[1] net4 dGND dGND dVDD dVDD D[6] sky130_fd_sc_hd__and4_1
x8 net1 A[2] net3 net4 dGND dGND dVDD dVDD D[4] sky130_fd_sc_hd__and4_1
x9 net1 net2 A[1] net4 dGND dGND dVDD dVDD D[2] sky130_fd_sc_hd__and4_1
x10 net1 net2 net3 net4 dGND dGND dVDD dVDD D[0] sky130_fd_sc_hd__and4_1
x11 net1 net2 net3 A[0] dGND dGND dVDD dVDD D[1] sky130_fd_sc_hd__and4_1
x12 net1 net2 A[1] A[0] dGND dGND dVDD dVDD D[3] sky130_fd_sc_hd__and4_1
x14 net1 A[2] net3 A[0] dGND dGND dVDD dVDD D[5] sky130_fd_sc_hd__and4_1
x1 A[3] dGND dGND dVDD dVDD net1 sky130_fd_sc_hd__inv_4
x2 A[2] dGND dGND dVDD dVDD net2 sky130_fd_sc_hd__inv_4
x3 A[1] dGND dGND dVDD dVDD net3 sky130_fd_sc_hd__inv_4
x7 A[0] dGND dGND dVDD dVDD net4 sky130_fd_sc_hd__inv_4
.ends


* expanding   symbol:  synapse_4bit_memory_v1_norail.sym # of pins=13
** sym_path: design/xschem/synapse_4bit_memory_v1_norail.sym
** sch_path: design/xschem/synapse_4bit_memory_v1_norail.sch
.subckt synapse_4bit_memory_v1_norail sout JExcWn[0] JExcWn[1] JExcWn[2] JExcWn[3] spk resetW
+ vpulseextp setW vthrdn W[0] W[1] W[2] W[3] vtaup VDD GND aVDD aGND
*.iopin GND
*.iopin VDD
*.ipin vpulseextp
*.ipin spk
*.ipin setW
*.ipin resetW
*.iopin sout
*.ipin vthrdn
*.ipin vtaup
*.iopin aVDD
*.ipin JExcWn[0],JExcWn[1],JExcWn[2],JExcWn[3]
*.ipin W[0],W[1],W[2],W[3]
*.iopin aGND
x2[0] setW W[0] net1 GND GND VDD VDD net2[3] sky130_fd_sc_hd__dfrtp_1
x2[1] setW W[1] net1 GND GND VDD VDD net2[2] sky130_fd_sc_hd__dfrtp_1
x2[2] setW W[2] net1 GND GND VDD VDD net2[1] sky130_fd_sc_hd__dfrtp_1
x2[3] setW W[3] net1 GND GND VDD VDD net2[0] sky130_fd_sc_hd__dfrtp_1
x4 resetW GND GND VDD VDD net1 sky130_fd_sc_hd__inv_1
x2 vtaup sout vthrdn spke JExcWn[0] JExcWn[1] JExcWn[2] JExcWn[3] aGND aVDD net2[3] net2[2] net2[1]
+ net2[0] dpi_syn_exc_4bit_fc_v2
x6 vpulseextp spk GND spke VDD spike_extender_with_trimming
x1 GND GND VDD VDD sky130_fd_sc_hd__decap_4
x3 GND GND VDD VDD sky130_fd_sc_hd__decap_3
x5 GND GND VDD VDD sky130_fd_sc_hd__decap_3
x7 GND GND VDD VDD sky130_fd_sc_hd__decap_6
x8 GND GND VDD VDD sky130_fd_sc_hd__decap_3
x9 GND GND VDD VDD sky130_fd_sc_hd__decap_3
.ends


* expanding   symbol:  synapse_4bit_memory_inh_v1_norail.sym # of pins=13
** sym_path: design/xschem/synapse_4bit_memory_inh_v1_norail.sym
** sch_path: design/xschem/synapse_4bit_memory_inh_v1_norail.sch
.subckt synapse_4bit_memory_inh_v1_norail sout JInhWp[0] JInhWp[1] JInhWp[2] JInhWp[3] resetW spk
+ vpulseextp setW vthrdp W[0] W[1] W[2] W[3] vtaun GND VDD aVDD aGND
*.ipin vpulseextp
*.ipin spk
*.ipin JInhWp[0],JInhWp[1],JInhWp[2],JInhWp[3]
*.ipin W[0],W[1],W[2],W[3]
*.ipin setW
*.ipin resetW
*.iopin sout
*.ipin vthrdp
*.ipin vtaun
*.iopin GND
*.iopin VDD
*.iopin aVDD
*.iopin aGND
x11 resetW GND GND VDD VDD net1 sky130_fd_sc_hd__inv_1
x2 JInhWp[0] JInhWp[1] JInhWp[2] JInhWp[3] net2[3] net2[2] net2[1] net2[0] spke sout vthrdp vtaun
+ aGND aVDD dpi_syn_inh_4bit_fc_v2
x2[0] setW W[0] net1 GND GND VDD VDD net3[3] net2[3] sky130_fd_sc_hd__dfrbp_1
x2[1] setW W[1] net1 GND GND VDD VDD net3[2] net2[2] sky130_fd_sc_hd__dfrbp_1
x2[2] setW W[2] net1 GND GND VDD VDD net3[1] net2[1] sky130_fd_sc_hd__dfrbp_1
x2[3] setW W[3] net1 GND GND VDD VDD net3[0] net2[0] sky130_fd_sc_hd__dfrbp_1
x4 vpulseextp spk GND spke VDD spike_extender_with_trimming
x1 GND GND VDD VDD sky130_fd_sc_hd__decap_4
.ends


* expanding   symbol:  dpi_syn_exc_4bit_fc_v2.sym # of pins=8
** sym_path: design/xschem/dpi_syn_exc_4bit_fc_v2.sym
** sch_path: design/xschem/dpi_syn_exc_4bit_fc_v2.sch
.subckt dpi_syn_exc_4bit_fc_v2 vtaup sout vthn spk JExcWn[0] JExcWn[1] JExcWn[2] JExcWn[3] GND aVDD
+ weight[0] weight[1] weight[2] weight[3]
*.iopin GND
*.iopin aVDD
*.iopin vtaup
*.ipin spk
*.opin sout
*.iopin vthn
*.ipin weight[0],weight[1],weight[2],weight[3]
*.iopin JExcWn[0],JExcWn[1],JExcWn[2],JExcWn[3]
XM2 net3 spk net1 GND sky130_fd_pr__nfet_01v8 L=0.25 W=1.0 nf=1 ad='int((nf+1)/2) * W/nf * 0.29' as='int((nf+2)/2) * W/nf * 0.29'
+ pd='2*int((nf+1)/2) * (W/nf + 0.29)' ps='2*int((nf+2)/2) * (W/nf + 0.29)' nrd='0.29 / W' nrs='0.29 / W'
+ sa=0 sb=0 sd=0 mult=1 m=1
XC1 vsin aVDD sky130_fd_pr__cap_mim_m3_1 W=5 L=5 MF=1 m=1
XM5 vsin vtaup aVDD aVDD sky130_fd_pr__pfet_01v8 L=0.2 W=1.2 nf=1 ad='int((nf+1)/2) * W/nf * 0.29' as='int((nf+2)/2) * W/nf * 0.29'
+ pd='2*int((nf+1)/2) * (W/nf + 0.29)' ps='2*int((nf+2)/2) * (W/nf + 0.29)' nrd='0.29 / W' nrs='0.29 / W'
+ sa=0 sb=0 sd=0 mult=1 m=1
XM6 sout vsin aVDD aVDD sky130_fd_pr__pfet_01v8 L=0.2 W=1.2 nf=1 ad='int((nf+1)/2) * W/nf * 0.29' as='int((nf+2)/2) * W/nf * 0.29'
+ pd='2*int((nf+1)/2) * (W/nf + 0.29)' ps='2*int((nf+2)/2) * (W/nf + 0.29)' nrd='0.29 / W' nrs='0.29 / W'
+ sa=0 sb=0 sd=0 mult=1 m=1
XM1 net1 JExcWn[0] net2 GND sky130_fd_pr__nfet_01v8 L=1.0 W=1.0 nf=1 ad='int((nf+1)/2) * W/nf * 0.29'
+ as='int((nf+2)/2) * W/nf * 0.29' pd='2*int((nf+1)/2) * (W/nf + 0.29)' ps='2*int((nf+2)/2) * (W/nf + 0.29)'
+ nrd='0.29 / W' nrs='0.29 / W' sa=0 sb=0 sd=0 mult=1 m=1
XM4 vsin vsin net3 GND sky130_fd_pr__nfet_01v8 L=0.25 W=1.0 nf=1 ad='int((nf+1)/2) * W/nf * 0.29' as='int((nf+2)/2) * W/nf * 0.29'
+ pd='2*int((nf+1)/2) * (W/nf + 0.29)' ps='2*int((nf+2)/2) * (W/nf + 0.29)' nrd='0.29 / W' nrs='0.29 / W'
+ sa=0 sb=0 sd=0 mult=1 m=1
XM3 aVDD vthn net3 GND sky130_fd_pr__nfet_01v8 L=0.25 W=1.0 nf=1 ad='int((nf+1)/2) * W/nf * 0.29' as='int((nf+2)/2) * W/nf * 0.29'
+ pd='2*int((nf+1)/2) * (W/nf + 0.29)' ps='2*int((nf+2)/2) * (W/nf + 0.29)' nrd='0.29 / W' nrs='0.29 / W'
+ sa=0 sb=0 sd=0 mult=1 m=1
XM7 net1 JExcWn[1] net4 GND sky130_fd_pr__nfet_01v8 L=2.0 W=1.0 nf=1 ad='int((nf+1)/2) * W/nf * 0.29'
+ as='int((nf+2)/2) * W/nf * 0.29' pd='2*int((nf+1)/2) * (W/nf + 0.29)' ps='2*int((nf+2)/2) * (W/nf + 0.29)'
+ nrd='0.29 / W' nrs='0.29 / W' sa=0 sb=0 sd=0 mult=1 m=1
XM8 net1 JExcWn[2] net5 GND sky130_fd_pr__nfet_01v8 L=4.0 W=1.0 nf=1 ad='int((nf+1)/2) * W/nf * 0.29'
+ as='int((nf+2)/2) * W/nf * 0.29' pd='2*int((nf+1)/2) * (W/nf + 0.29)' ps='2*int((nf+2)/2) * (W/nf + 0.29)'
+ nrd='0.29 / W' nrs='0.29 / W' sa=0 sb=0 sd=0 mult=1 m=1
XM9 net1 JExcWn[3] net6 GND sky130_fd_pr__nfet_01v8 L=8.0 W=1.0 nf=1 ad='int((nf+1)/2) * W/nf * 0.29'
+ as='int((nf+2)/2) * W/nf * 0.29' pd='2*int((nf+1)/2) * (W/nf + 0.29)' ps='2*int((nf+2)/2) * (W/nf + 0.29)'
+ nrd='0.29 / W' nrs='0.29 / W' sa=0 sb=0 sd=0 mult=1 m=1
XM10 net2 weight[0] GND GND sky130_fd_pr__nfet_01v8 L=0.25 W=1.0 nf=1 ad='int((nf+1)/2) * W/nf * 0.29'
+ as='int((nf+2)/2) * W/nf * 0.29' pd='2*int((nf+1)/2) * (W/nf + 0.29)' ps='2*int((nf+2)/2) * (W/nf + 0.29)'
+ nrd='0.29 / W' nrs='0.29 / W' sa=0 sb=0 sd=0 mult=1 m=1
XM11 net4 weight[1] GND GND sky130_fd_pr__nfet_01v8 L=0.25 W=1.0 nf=1 ad='int((nf+1)/2) * W/nf * 0.29'
+ as='int((nf+2)/2) * W/nf * 0.29' pd='2*int((nf+1)/2) * (W/nf + 0.29)' ps='2*int((nf+2)/2) * (W/nf + 0.29)'
+ nrd='0.29 / W' nrs='0.29 / W' sa=0 sb=0 sd=0 mult=1 m=1
XM12 net5 weight[2] GND GND sky130_fd_pr__nfet_01v8 L=0.25 W=1.0 nf=1 ad='int((nf+1)/2) * W/nf * 0.29'
+ as='int((nf+2)/2) * W/nf * 0.29' pd='2*int((nf+1)/2) * (W/nf + 0.29)' ps='2*int((nf+2)/2) * (W/nf + 0.29)'
+ nrd='0.29 / W' nrs='0.29 / W' sa=0 sb=0 sd=0 mult=1 m=1
XM13 net6 weight[3] GND GND sky130_fd_pr__nfet_01v8 L=0.25 W=1.0 nf=1 ad='int((nf+1)/2) * W/nf * 0.29'
+ as='int((nf+2)/2) * W/nf * 0.29' pd='2*int((nf+1)/2) * (W/nf + 0.29)' ps='2*int((nf+2)/2) * (W/nf + 0.29)'
+ nrd='0.29 / W' nrs='0.29 / W' sa=0 sb=0 sd=0 mult=1 m=1
.ends


* expanding   symbol:  spike_extender_with_trimming.sym # of pins=5
** sym_path: design/xschem/spike_extender_with_trimming.sym
** sch_path: design/xschem/spike_extender_with_trimming.sch
.subckt spike_extender_with_trimming vpulseextp vspk GND spkext VDD
*.iopin GND
*.iopin VDD
*.ipin vspk
*.opin spkext
*.ipin vpulseextp
x1 vpulseextp vpulseshort GND spkext VDD spike_extender
x3 vspk GND GND VDD VDD net1 sky130_fd_sc_hd__clkdlybuf4s50_1
x2 net1 vspk GND GND VDD VDD vpulseshort sky130_fd_sc_hd__nor2b_1
.ends


* expanding   symbol:  dpi_syn_inh_4bit_fc_v2.sym # of pins=8
** sym_path: design/xschem/dpi_syn_inh_4bit_fc_v2.sym
** sch_path: design/xschem/dpi_syn_inh_4bit_fc_v2.sch
.subckt dpi_syn_inh_4bit_fc_v2 JInhWp[0] JInhWp[1] JInhWp[2] JInhWp[3] weight_b[0] weight_b[1]
+ weight_b[2] weight_b[3] spk sout vthrdp vtaun GND aVDD
*.ipin spk
*.iopin vthrdp
*.iopin vtaun
*.iopin sout
*.iopin GND
*.iopin aVDD
*.ipin weight_b[0],weight_b[1],weight_b[2],weight_b[3]
*.iopin JInhWp[0],JInhWp[1],JInhWp[2],JInhWp[3]
XM5 net2 net3 net1 aVDD sky130_fd_pr__pfet_01v8 L=0.2 W=1.2 nf=1 ad='int((nf+1)/2) * W/nf * 0.29' as='int((nf+2)/2) * W/nf * 0.29'
+ pd='2*int((nf+1)/2) * (W/nf + 0.29)' ps='2*int((nf+2)/2) * (W/nf + 0.29)' nrd='0.29 / W' nrs='0.29 / W'
+ sa=0 sb=0 sd=0 mult=1 m=1
XM2 GND vthrdp net2 aVDD sky130_fd_pr__pfet_01v8 L=0.2 W=1.2 nf=1 ad='int((nf+1)/2) * W/nf * 0.29' as='int((nf+2)/2) * W/nf * 0.29'
+ pd='2*int((nf+1)/2) * (W/nf + 0.29)' ps='2*int((nf+2)/2) * (W/nf + 0.29)' nrd='0.29 / W' nrs='0.29 / W'
+ sa=0 sb=0 sd=0 mult=1 m=1
XM3 vsin vsin net2 aVDD sky130_fd_pr__pfet_01v8 L=0.2 W=1.2 nf=1 ad='int((nf+1)/2) * W/nf * 0.29' as='int((nf+2)/2) * W/nf * 0.29'
+ pd='2*int((nf+1)/2) * (W/nf + 0.29)' ps='2*int((nf+2)/2) * (W/nf + 0.29)' nrd='0.29 / W' nrs='0.29 / W'
+ sa=0 sb=0 sd=0 mult=1 m=1
XM4 vsin vtaun GND GND sky130_fd_pr__nfet_01v8 L=0.25 W=1.0 nf=1 ad='int((nf+1)/2) * W/nf * 0.29' as='int((nf+2)/2) * W/nf * 0.29'
+ pd='2*int((nf+1)/2) * (W/nf + 0.29)' ps='2*int((nf+2)/2) * (W/nf + 0.29)' nrd='0.29 / W' nrs='0.29 / W'
+ sa=0 sb=0 sd=0 mult=1 m=1
XM6 sout vsin GND GND sky130_fd_pr__nfet_01v8 L=0.25 W=1.0 nf=1 ad='int((nf+1)/2) * W/nf * 0.29' as='int((nf+2)/2) * W/nf * 0.29'
+ pd='2*int((nf+1)/2) * (W/nf + 0.29)' ps='2*int((nf+2)/2) * (W/nf + 0.29)' nrd='0.29 / W' nrs='0.29 / W'
+ sa=0 sb=0 sd=0 mult=1 m=1
XM7 net3 spk GND GND sky130_fd_pr__nfet_01v8 L=0.25 W=1.0 nf=1 ad='int((nf+1)/2) * W/nf * 0.29' as='int((nf+2)/2) * W/nf * 0.29'
+ pd='2*int((nf+1)/2) * (W/nf + 0.29)' ps='2*int((nf+2)/2) * (W/nf + 0.29)' nrd='0.29 / W' nrs='0.29 / W'
+ sa=0 sb=0 sd=0 mult=1 m=1
XM8 net3 spk aVDD aVDD sky130_fd_pr__pfet_01v8 L=0.2 W=1.2 nf=1 ad='int((nf+1)/2) * W/nf * 0.29' as='int((nf+2)/2) * W/nf * 0.29'
+ pd='2*int((nf+1)/2) * (W/nf + 0.29)' ps='2*int((nf+2)/2) * (W/nf + 0.29)' nrd='0.29 / W' nrs='0.29 / W'
+ sa=0 sb=0 sd=0 mult=1 m=1
XC1 vsin GND sky130_fd_pr__cap_mim_m3_1 W=5 L=5 MF=1 m=1
XM9 net4 JInhWp[0] aVDD aVDD sky130_fd_pr__pfet_01v8 L=1.2 W=1.2 nf=1 ad='int((nf+1)/2) * W/nf * 0.29'
+ as='int((nf+2)/2) * W/nf * 0.29' pd='2*int((nf+1)/2) * (W/nf + 0.29)' ps='2*int((nf+2)/2) * (W/nf + 0.29)'
+ nrd='0.29 / W' nrs='0.29 / W' sa=0 sb=0 sd=0 mult=1 m=1
XM10 net1 weight_b[0] net4 aVDD sky130_fd_pr__pfet_01v8 L=0.2 W=1.2 nf=1 ad='int((nf+1)/2) * W/nf * 0.29'
+ as='int((nf+2)/2) * W/nf * 0.29' pd='2*int((nf+1)/2) * (W/nf + 0.29)' ps='2*int((nf+2)/2) * (W/nf + 0.29)'
+ nrd='0.29 / W' nrs='0.29 / W' sa=0 sb=0 sd=0 mult=1 m=1
XM11 net1 weight_b[1] net5 aVDD sky130_fd_pr__pfet_01v8 L=0.2 W=1.2 nf=1 ad='int((nf+1)/2) * W/nf * 0.29'
+ as='int((nf+2)/2) * W/nf * 0.29' pd='2*int((nf+1)/2) * (W/nf + 0.29)' ps='2*int((nf+2)/2) * (W/nf + 0.29)'
+ nrd='0.29 / W' nrs='0.29 / W' sa=0 sb=0 sd=0 mult=1 m=1
XM1 net5 JInhWp[1] aVDD aVDD sky130_fd_pr__pfet_01v8 L=2.0 W=1.2 nf=1 ad='int((nf+1)/2) * W/nf * 0.29'
+ as='int((nf+2)/2) * W/nf * 0.29' pd='2*int((nf+1)/2) * (W/nf + 0.29)' ps='2*int((nf+2)/2) * (W/nf + 0.29)'
+ nrd='0.29 / W' nrs='0.29 / W' sa=0 sb=0 sd=0 mult=1 m=1
XM12 net6 JInhWp[2] aVDD aVDD sky130_fd_pr__pfet_01v8 L=4.0 W=1.2 nf=1 ad='int((nf+1)/2) * W/nf * 0.29'
+ as='int((nf+2)/2) * W/nf * 0.29' pd='2*int((nf+1)/2) * (W/nf + 0.29)' ps='2*int((nf+2)/2) * (W/nf + 0.29)'
+ nrd='0.29 / W' nrs='0.29 / W' sa=0 sb=0 sd=0 mult=1 m=1
XM13 net7 JInhWp[3] aVDD aVDD sky130_fd_pr__pfet_01v8 L=8.0 W=1.2 nf=1 ad='int((nf+1)/2) * W/nf * 0.29'
+ as='int((nf+2)/2) * W/nf * 0.29' pd='2*int((nf+1)/2) * (W/nf + 0.29)' ps='2*int((nf+2)/2) * (W/nf + 0.29)'
+ nrd='0.29 / W' nrs='0.29 / W' sa=0 sb=0 sd=0 mult=1 m=1
XM14 net1 weight_b[2] net6 aVDD sky130_fd_pr__pfet_01v8 L=0.2 W=1.2 nf=1 ad='int((nf+1)/2) * W/nf * 0.29'
+ as='int((nf+2)/2) * W/nf * 0.29' pd='2*int((nf+1)/2) * (W/nf + 0.29)' ps='2*int((nf+2)/2) * (W/nf + 0.29)'
+ nrd='0.29 / W' nrs='0.29 / W' sa=0 sb=0 sd=0 mult=1 m=1
XM15 net1 weight_b[3] net7 aVDD sky130_fd_pr__pfet_01v8 L=0.2 W=1.2 nf=1 ad='int((nf+1)/2) * W/nf * 0.29'
+ as='int((nf+2)/2) * W/nf * 0.29' pd='2*int((nf+1)/2) * (W/nf + 0.29)' ps='2*int((nf+2)/2) * (W/nf + 0.29)'
+ nrd='0.29 / W' nrs='0.29 / W' sa=0 sb=0 sd=0 mult=1 m=1
.ends


* expanding   symbol:  spike_extender.sym # of pins=5
** sym_path: design/xschem/spike_extender.sym
** sch_path: design/xschem/spike_extender.sch
.subckt spike_extender vpulseextp spk GND spkext VDD
*.iopin GND
*.iopin VDD
*.ipin spk
*.opin spkext
*.ipin vpulseextp
XM1 net1 spk GND GND sky130_fd_pr__nfet_01v8 L=0.15 W=0.65 nf=1 ad='int((nf+1)/2) * W/nf * 0.29' as='int((nf+2)/2) * W/nf * 0.29'
+ pd='2*int((nf+1)/2) * (W/nf + 0.29)' ps='2*int((nf+2)/2) * (W/nf + 0.29)' nrd='0.29 / W' nrs='0.29 / W'
+ sa=0 sb=0 sd=0 mult=1 m=1
XM6 net1 vpulseextp VDD VDD sky130_fd_pr__pfet_01v8 L=2 W=1 nf=1 ad='int((nf+1)/2) * W/nf * 0.29' as='int((nf+2)/2) * W/nf * 0.29'
+ pd='2*int((nf+1)/2) * (W/nf + 0.29)' ps='2*int((nf+2)/2) * (W/nf + 0.29)' nrd='0.29 / W' nrs='0.29 / W'
+ sa=0 sb=0 sd=0 mult=1 m=1
XM5 net3 net2 GND GND sky130_fd_pr__nfet_01v8 L=0.15 W=0.65 nf=1 ad='int((nf+1)/2) * W/nf * 0.29' as='int((nf+2)/2) * W/nf * 0.29'
+ pd='2*int((nf+1)/2) * (W/nf + 0.29)' ps='2*int((nf+2)/2) * (W/nf + 0.29)' nrd='0.29 / W' nrs='0.29 / W'
+ sa=0 sb=0 sd=0 mult=1 m=1
XM8 spkext net3 GND GND sky130_fd_pr__nfet_01v8 L=0.15 W=0.65 nf=1 ad='int((nf+1)/2) * W/nf * 0.29' as='int((nf+2)/2) * W/nf * 0.29'
+ pd='2*int((nf+1)/2) * (W/nf + 0.29)' ps='2*int((nf+2)/2) * (W/nf + 0.29)' nrd='0.29 / W' nrs='0.29 / W'
+ sa=0 sb=0 sd=0 mult=1 m=1
XM4 net3 net2 VDD VDD sky130_fd_pr__pfet_01v8 L=0.15 W=1.0 nf=1 ad='int((nf+1)/2) * W/nf * 0.29' as='int((nf+2)/2) * W/nf * 0.29'
+ pd='2*int((nf+1)/2) * (W/nf + 0.29)' ps='2*int((nf+2)/2) * (W/nf + 0.29)' nrd='0.29 / W' nrs='0.29 / W'
+ sa=0 sb=0 sd=0 mult=1 m=1
XM7 spkext net3 VDD VDD sky130_fd_pr__pfet_01v8 L=0.15 W=1.0 nf=1 ad='int((nf+1)/2) * W/nf * 0.29' as='int((nf+2)/2) * W/nf * 0.29'
+ pd='2*int((nf+1)/2) * (W/nf + 0.29)' ps='2*int((nf+2)/2) * (W/nf + 0.29)' nrd='0.29 / W' nrs='0.29 / W'
+ sa=0 sb=0 sd=0 mult=1 m=1
XM2 net2 net1 GND GND sky130_fd_pr__nfet_01v8 L=0.15 W=0.65 nf=1 ad='int((nf+1)/2) * W/nf * 0.29' as='int((nf+2)/2) * W/nf * 0.29'
+ pd='2*int((nf+1)/2) * (W/nf + 0.29)' ps='2*int((nf+2)/2) * (W/nf + 0.29)' nrd='0.29 / W' nrs='0.29 / W'
+ sa=0 sb=0 sd=0 mult=1 m=1
XM3 net2 net1 VDD VDD sky130_fd_pr__pfet_01v8 L=0.15 W=1.0 nf=1 ad='int((nf+1)/2) * W/nf * 0.29' as='int((nf+2)/2) * W/nf * 0.29'
+ pd='2*int((nf+1)/2) * (W/nf + 0.29)' ps='2*int((nf+2)/2) * (W/nf + 0.29)' nrd='0.29 / W' nrs='0.29 / W'
+ sa=0 sb=0 sd=0 mult=1 m=1
XM9 GND net1 GND GND sky130_fd_pr__nfet_01v8 L=1 W=0.65 nf=1 ad='int((nf+1)/2) * W/nf * 0.29' as='int((nf+2)/2) * W/nf * 0.29'
+ pd='2*int((nf+1)/2) * (W/nf + 0.29)' ps='2*int((nf+2)/2) * (W/nf + 0.29)' nrd='0.29 / W' nrs='0.29 / W'
+ sa=0 sb=0 sd=0 mult=1 m=1
.ends

.end
